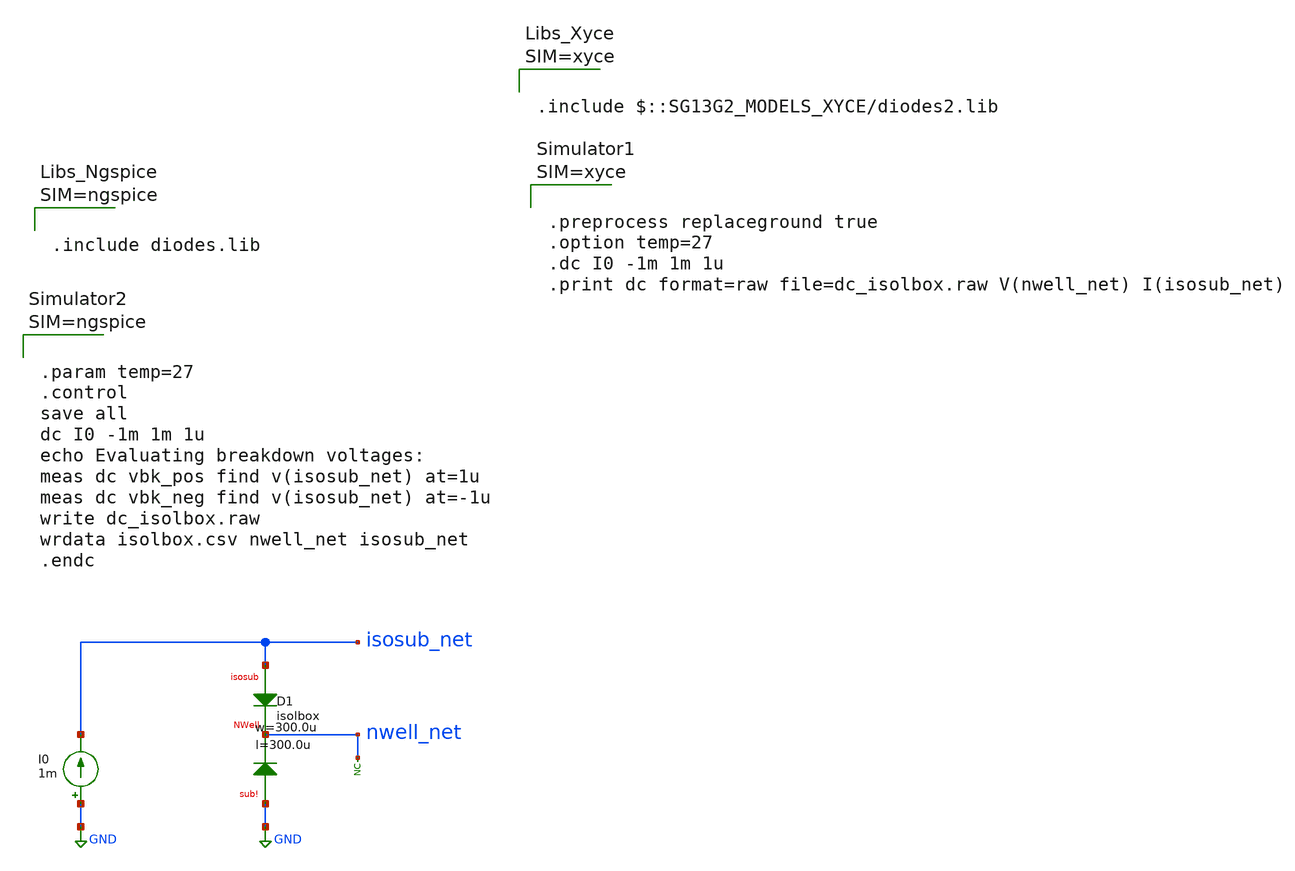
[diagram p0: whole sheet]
** sch_path: ihp-sg13g2/libs.tech/xschem/sg13g2_tests_xyce/dc_isolbox.sch
* Copyright 2023 IHP PDK Authors
**.subckt dc_isolbox
I0 GND isosub_net 1m
XD1 isosub_net nwell_net GND isolbox l=300.0u w=300.0u
* noconn nwell_net
**** begin user architecture code









.include diodes.lib






.param temp=27
.control
save all
dc I0 -1m 1m 1u
echo Evaluating breakdown voltages:
meas dc vbk_pos find v(isosub_net) at=1u
meas dc vbk_neg find v(isosub_net) at=-1u
write dc_isolbox.raw
wrdata isolbox.csv nwell_net isosub_net
.endc



**** end user architecture code
**.ends
.GLOBAL GND
.end
